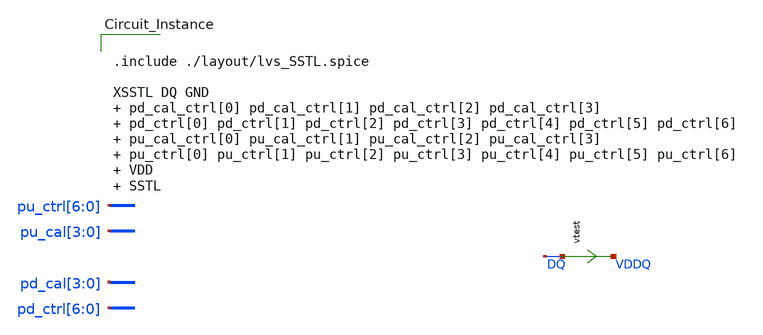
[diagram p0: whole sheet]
** sch_path: schem/post_layout_sstl_res_tb.sch
* Copyright 2021 Stefan Frederik Schippers
* Licensed under the Apache License, Version 2.0 (the "License");
* you may not use this file except in compliance with the License.
* You may obtain a copy of the License at
* https://www.apache.org/licenses/LICENSE-2.0
* Unless required by applicable law or agreed to in writing, software
* distributed under the License is distributed on an "AS IS" BASIS,
* WITHOUT WARRANTIES OR CONDITIONS OF ANY KIND, either express or implied.
* See the License for the specific language governing permissions and
* limitations under the License.
**.subckt post_layout_sstl_res_tb
vtest DQ VDDQ 0
.save i(vtest)
**** begin user architecture code
 ** Local library links to pdk
.lib ./sky130/libs/SED_process_SED_lib.spice SED_process_SED
.include $::SKYWATER_STDCELLS/sky130_fd_sc_hd.spice



.include ./layout/lvs_SSTL.spice

XSSTL DQ GND   pd_cal_ctrl[0] pd_cal_ctrl[1] pd_cal_ctrl[2] pd_cal_ctrl[3]  pd_ctrl[0] pd_ctrl[1]
+ pd_ctrl[2] pd_ctrl[3] pd_ctrl[4] pd_ctrl[5] pd_ctrl[6]   pu_cal_ctrl[0] pu_cal_ctrl[1] pu_cal_ctrl[2]
+ pu_cal_ctrl[3]   pu_ctrl[0] pu_ctrl[1] pu_ctrl[2] pu_ctrl[3] pu_ctrl[4] pu_ctrl[5] pu_ctrl[6]   VDD  SSTL


**** end user architecture code
**.ends
**** begin user architecture code


* power voltage
vvddq VDDQ 0 0
vvdd VDD 0 SED_vdd_SED

** CALIBRATION CONTROL **
* PULLUP
vpu_cal0 pu_cal[0] 0 SED_pucal0_SED
vpu_cal1 pu_cal[1] 0 SED_pucal1_SED
vpu_cal2 pu_cal[2] 0 SED_pucal2_SED
vpu_cal3 pu_cal[3] 0 SED_pucal3_SED
* PULLDOWN
vpd_cal0 pd_cal[0] 0 SED_pdcal0_SED
vpd_cal1 pd_cal[1] 0 SED_pdcal1_SED
vpd_cal2 pd_cal[2] 0 SED_pdcal2_SED
vpd_cal3 pd_cal[3] 0 SED_pdcal3_SED

** LEG ENABLE/DISABLE CONTROL
* PULLUP
vpu_ctrl0 pu_ctrl[0] 0 SED_puctrl0_SED
vpu_ctrl1 pu_ctrl[1] 0 SED_puctrl1_SED
vpu_ctrl2 pu_ctrl[2] 0 SED_puctrl2_SED
vpu_ctrl3 pu_ctrl[3] 0 SED_puctrl3_SED
vpu_ctrl4 pu_ctrl[4] 0 SED_puctrl4_SED
vpu_ctrl5 pu_ctrl[5] 0 SED_puctrl5_SED
vpu_ctrl6 pu_ctrl[6] 0 SED_puctrl6_SED
* PULLDOWN
vpd_ctrl0 pd_ctrl[0] 0 SED_pdctrl0_SED
vpd_ctrl1 pd_ctrl[1] 0 SED_pdctrl1_SED
vpd_ctrl2 pd_ctrl[2] 0 SED_pdctrl2_SED
vpd_ctrl3 pd_ctrl[3] 0 SED_pdctrl3_SED
vpd_ctrl4 pd_ctrl[4] 0 SED_pdctrl4_SED
vpd_ctrl5 pd_ctrl[5] 0 SED_pdctrl5_SED
vpd_ctrl6 pd_ctrl[6] 0 SED_pdctrl6_SED


.control
set num_threads=1
save all
set temp=SED_temp_SED

* RUN SIMULATION
dc vvddq 0.3 1.2 0.05
* OUTPUT
print i(vtest)
wrdata out/SED_plotName_SED/SED_plotName_SED.txt i(vtest)
set hcopydevtype = svg
hardcopy ./out/SED_plotName_SED/SED_plotName_SED.svg I(vtest) vs vddq title 'Resistance vs pin voltage'

.endc


**** end user architecture code
.end
